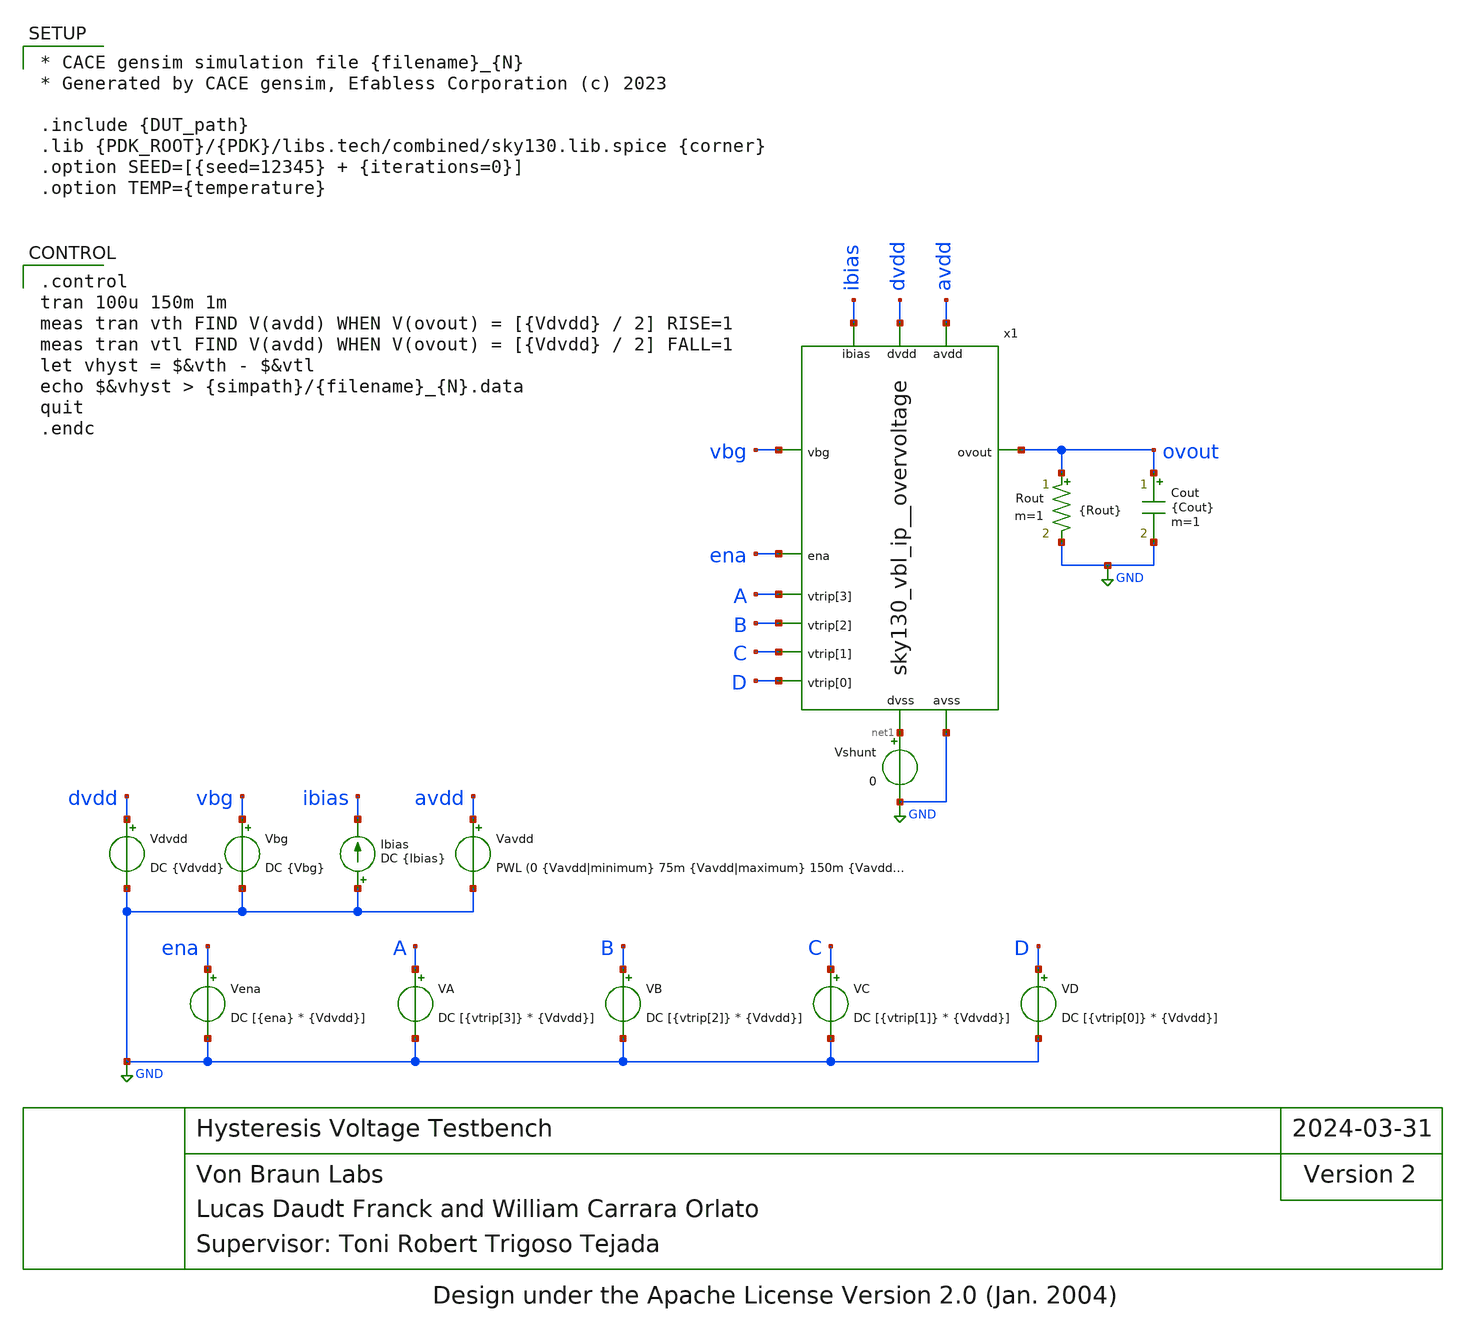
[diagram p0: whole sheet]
** sch_path: cace/tb_vhyst.sch
* Design under the Apache License Version 2.0 (Jan. 2004)
**.subckt tb_vhyst
Vavdd avdd GND PWL (0 {Vavdd|minimum} 75m {Vavdd|maximum} 150m {Vavdd|minimum})
Vdvdd dvdd GND DC {Vdvdd}
Vbg vbg GND DC {Vbg}
Ibias GND ibias DC {Ibias}
Vena ena GND DC [{ena} * {Vdvdd}]
VA A GND DC [{vtrip[3]} * {Vdvdd}]
VB B GND DC [{vtrip[2]} * {Vdvdd}]
VC C GND DC [{vtrip[1]} * {Vdvdd}]
VD D GND DC [{vtrip[0]} * {Vdvdd}]
Cout ovout GND {Cout} m=1
Rout ovout GND {Rout} m=1
x1 avdd dvdd ena A ibias B ovout vbg C D net1 GND sky130_vbl_ip__overvoltage
Vshunt net1 GND 0
**** begin user architecture code

* CACE gensim simulation file {filename}_{N}
* Generated by CACE gensim, Efabless Corporation (c) 2023

.include {DUT_path}
.lib {PDK_ROOT}/{PDK}/libs.tech/combined/sky130.lib.spice {corner}
.option SEED=[{seed=12345} + {iterations=0}]
.option TEMP={temperature}



.control
tran 100u 150m 1m
meas tran vth FIND V(avdd) WHEN V(ovout) = [{Vdvdd} / 2] RISE=1
meas tran vtl FIND V(avdd) WHEN V(ovout) = [{Vdvdd} / 2] FALL=1
let vhyst = $&vth - $&vtl
echo $&vhyst > {simpath}/{filename}_{N}.data
quit
.endc


**** end user architecture code
**.ends
.GLOBAL GND
.end
